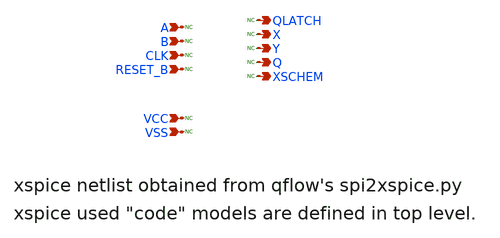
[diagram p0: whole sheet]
** sch_path: sky130A/xschem_libs/sky130_tests_ase/stdcells_xspice/schematic/stdcells_xspice.sch
* Copyright 2021 Stefan Frederik Schippers
* Licensed under the Apache License, Version 2.0 (the "License");
* you may not use this file except in compliance with the License.
* You may obtain a copy of the License at
* https://www.apache.org/licenses/LICENSE-2.0
* Unless required by applicable law or agreed to in writing, software
* distributed under the License is distributed on an "AS IS" BASIS,
* WITHOUT WARRANTIES OR CONDITIONS OF ANY KIND, either express or implied.
* See the License for the specific language governing permissions and
* limitations under the License.
**.subckt stdcells_xspice RESET_B CLK B A Y X QLATCH Q XSCHEM VCC VSS
*.ipin RESET_B
*.ipin CLK
*.ipin B
*.ipin A
*.opin Y
*.opin X
*.opin QLATCH
*.opin Q
*.opin XSCHEM
*.ipin VCC
*.ipin VSS
* noconn A
* noconn B
* noconn CLK
* noconn RESET_B
* noconn VCC
* noconn VSS
* noconn QLATCH
* noconn X
* noconn Y
* noconn Q
* noconn XSCHEM
**** begin user architecture code


A1 [A B] IX d_lut_sky130_fd_sc_hd__nand2_1
A2 A CLK NULL ~RESET_B IQ NULL ddflop
A3 [A B] IY d_lut_sky130_fd_sc_hd__nor2b_1
A4 A ~CLK NULL ~RESET_B IQLATCH net1 dlatch
A5 [IY B] net2 d_lut_sky130_fd_sc_hd__nor2b_1
A6 [net2 IQLATCH] net4 d_lut_sky130_fd_sc_hd__nand2_1
A7 [net3 net4 IQ RESET_B] IXSCHEM d_lut_sky130_fd_sc_hd__a31o_2
A8 [IY] net3 d_lut_sky130_fd_sc_hd__inv_2
A13 [IY] Y d_lut_sky130_fd_sc_hd__buf_2
A9 [IX] X d_lut_sky130_fd_sc_hd__buf_2
A14 [IQ] Q d_lut_sky130_fd_sc_hd__buf_2
A15 [IQLATCH] QLATCH d_lut_sky130_fd_sc_hd__buf_2
A11 [IXSCHEM] XSCHEM d_lut_sky130_fd_sc_hd__buf_2


**** end user architecture code
**.ends
.end
